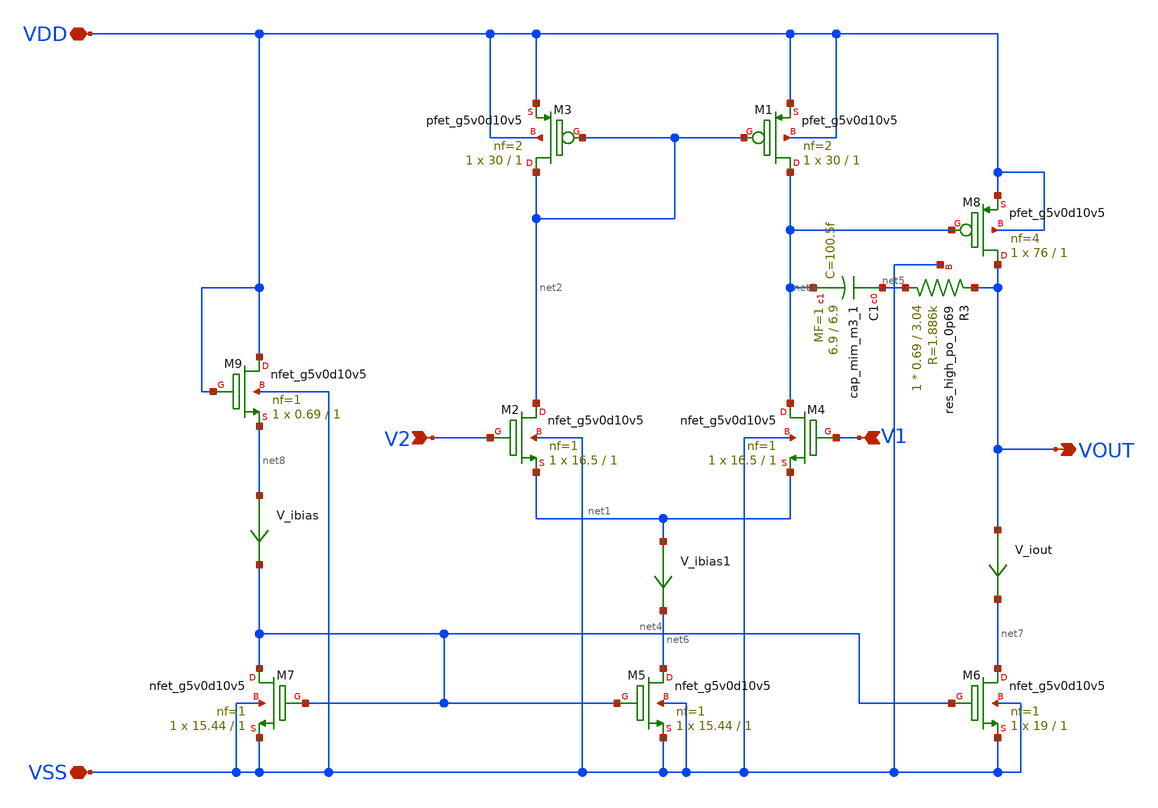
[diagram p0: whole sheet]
** sch_path: xschem/opamp.sch
**.subckt opamp VSS VDD V2 V1 VOUT
*.iopin VSS
*.iopin VDD
*.ipin V2
*.ipin V1
*.opin VOUT
XM2 net2 V2 net1 VSS sky130_fd_pr__nfet_g5v0d10v5 L=1 W=16.5 nf=1 ad='int((nf+1)/2) * W/nf * 0.29' as='int((nf+2)/2) * W/nf * 0.29'
+ pd='2*int((nf+1)/2) * (W/nf + 0.29)' ps='2*int((nf+2)/2) * (W/nf + 0.29)' nrd='0.29 / W' nrs='0.29 / W'
+ sa=0 sb=0 sd=0 mult=1 m=1
XM1 net3 net2 VDD VDD sky130_fd_pr__pfet_g5v0d10v5 L=1 W=30 nf=2 ad='int((nf+1)/2) * W/nf * 0.29' as='int((nf+2)/2) * W/nf * 0.29'
+ pd='2*int((nf+1)/2) * (W/nf + 0.29)' ps='2*int((nf+2)/2) * (W/nf + 0.29)' nrd='0.29 / W' nrs='0.29 / W'
+ sa=0 sb=0 sd=0 mult=1 m=1
XM4 net3 V1 net1 VSS sky130_fd_pr__nfet_g5v0d10v5 L=1 W=16.5 nf=1 ad='int((nf+1)/2) * W/nf * 0.29' as='int((nf+2)/2) * W/nf * 0.29'
+ pd='2*int((nf+1)/2) * (W/nf + 0.29)' ps='2*int((nf+2)/2) * (W/nf + 0.29)' nrd='0.29 / W' nrs='0.29 / W'
+ sa=0 sb=0 sd=0 mult=1 m=1
XM5 net6 net4 VSS VSS sky130_fd_pr__nfet_g5v0d10v5 L=1 W=15.44 nf=1 ad='int((nf+1)/2) * W/nf * 0.29'
+ as='int((nf+2)/2) * W/nf * 0.29' pd='2*int((nf+1)/2) * (W/nf + 0.29)' ps='2*int((nf+2)/2) * (W/nf + 0.29)'
+ nrd='0.29 / W' nrs='0.29 / W' sa=0 sb=0 sd=0 mult=1 m=1
XM6 net7 net4 VSS VSS sky130_fd_pr__nfet_g5v0d10v5 L=1 W=19 nf=1 ad='int((nf+1)/2) * W/nf * 0.29' as='int((nf+2)/2) * W/nf * 0.29'
+ pd='2*int((nf+1)/2) * (W/nf + 0.29)' ps='2*int((nf+2)/2) * (W/nf + 0.29)' nrd='0.29 / W' nrs='0.29 / W'
+ sa=0 sb=0 sd=0 mult=1 m=1
XM7 net4 net4 VSS VSS sky130_fd_pr__nfet_g5v0d10v5 L=1 W=15.44 nf=1 ad='int((nf+1)/2) * W/nf * 0.29'
+ as='int((nf+2)/2) * W/nf * 0.29' pd='2*int((nf+1)/2) * (W/nf + 0.29)' ps='2*int((nf+2)/2) * (W/nf + 0.29)'
+ nrd='0.29 / W' nrs='0.29 / W' sa=0 sb=0 sd=0 mult=1 m=1
XM3 net2 net2 VDD VDD sky130_fd_pr__pfet_g5v0d10v5 L=1 W=30 nf=2 ad='int((nf+1)/2) * W/nf * 0.29' as='int((nf+2)/2) * W/nf * 0.29'
+ pd='2*int((nf+1)/2) * (W/nf + 0.29)' ps='2*int((nf+2)/2) * (W/nf + 0.29)' nrd='0.29 / W' nrs='0.29 / W'
+ sa=0 sb=0 sd=0 mult=1 m=1
XM8 VOUT net3 VDD VDD sky130_fd_pr__pfet_g5v0d10v5 L=1 W=76 nf=4 ad='int((nf+1)/2) * W/nf * 0.29' as='int((nf+2)/2) * W/nf * 0.29'
+ pd='2*int((nf+1)/2) * (W/nf + 0.29)' ps='2*int((nf+2)/2) * (W/nf + 0.29)' nrd='0.29 / W' nrs='0.29 / W'
+ sa=0 sb=0 sd=0 mult=1 m=1
XC1 net5 net3 sky130_fd_pr__cap_mim_m3_1 W=6.9 L=6.9 MF=1 m=1
V_ibias net8 net4 0
.save i(v_ibias)
XR3 net5 VOUT VSS sky130_fd_pr__res_high_po_0p69 L=3.04 mult=1 m=1
V_ibias1 net1 net6 0
.save i(v_ibias1)
V_iout VOUT net7 0
.save i(v_iout)
XM9 VDD VDD net8 VSS sky130_fd_pr__nfet_g5v0d10v5 L=1 W=0.69 nf=1 ad='int((nf+1)/2) * W/nf * 0.29' as='int((nf+2)/2) * W/nf * 0.29'
+ pd='2*int((nf+1)/2) * (W/nf + 0.29)' ps='2*int((nf+2)/2) * (W/nf + 0.29)' nrd='0.29 / W' nrs='0.29 / W'
+ sa=0 sb=0 sd=0 mult=1 m=1
**.ends
.end
